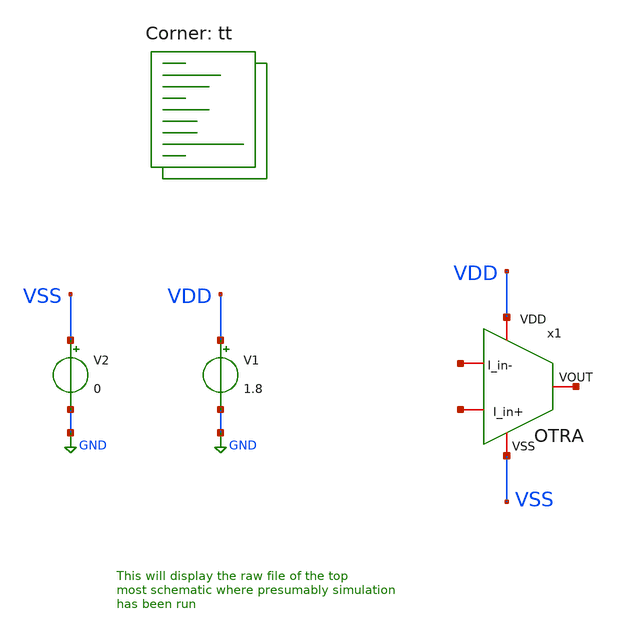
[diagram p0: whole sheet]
** sch_path: my_ip/sky130A/OTRA_VGA/testbenches/tb.sch
**.subckt tb
V1 VDD GND 1.8
V2 VSS GND 0
x1 VDD VSS net1 net2 net3 OTRA
**** begin user architecture code
.lib $::SKYWATER_MODELS/sky130.lib.spice tt
**** end user architecture code
**.ends
.GLOBAL GND
**** begin user architecture code


* ngspice commands
.options savecurrents
.TEMP 27
.control
save all
save @m.x1.xm1.msky130_fd_pr__pfet_01v8_lvt[gm]
save @m.x1.xm1.msky130_fd_pr__pfet_01v8_lvt[vth]
save @m.x1.xm1.msky130_fd_pr__pfet_01v8_lvt[gds]
save @m.x1.xm1.msky130_fd_pr__pfet_01v8_lvt[gmbs]
save @m.x1.xm1.msky130_fd_pr__pfet_01v8_lvt[vds]
save @m.x1.xm1.msky130_fd_pr__pfet_01v8_lvt[vgs]


save @m.x1.xm2.msky130_fd_pr__pfet_01v8_lvt[gm]
save @m.x1.xm2.msky130_fd_pr__pfet_01v8_lvt[vth]
save @m.x1.xm2.msky130_fd_pr__pfet_01v8_lvt[gds]
save @m.x1.xm2.msky130_fd_pr__pfet_01v8_lvt[gmbs]
save @m.x1.xm2.msky130_fd_pr__pfet_01v8_lvt[vds]
save @m.x1.xm2.msky130_fd_pr__pfet_01v8_lvt[vgs]

save @m.x1.xm3.msky130_fd_pr__nfet_01v8[gm]
save @m.x1.xm3.msky130_fd_pr__nfet_01v8[vth]
save @m.x1.xm3.msky130_fd_pr__nfet_01v8[gds]
save @m.x1.xm3.msky130_fd_pr__nfet_01v8[gmbs]
save @m.x1.xm3.msky130_fd_pr__nfet_01v8[vds]
save @m.x1.xm3.msky130_fd_pr__nfet_01v8[vgs]

save @m.x1.xm4.msky130_fd_pr__nfet_01v8[gm]
save @m.x1.xm4.msky130_fd_pr__nfet_01v8[vth]
save @m.x1.xm4.msky130_fd_pr__nfet_01v8[gds]
save @m.x1.xm4.msky130_fd_pr__nfet_01v8[gmbs]
save @m.x1.xm4.msky130_fd_pr__nfet_01v8[vds]
save @m.x1.xm4.msky130_fd_pr__nfet_01v8[vgs]

save @m.x1.xm5.msky130_fd_pr__nfet_01v8[gm]
save @m.x1.xm5.msky130_fd_pr__nfet_01v8[vth]
save @m.x1.xm5.msky130_fd_pr__nfet_01v8[gds]
save @m.x1.xm5.msky130_fd_pr__nfet_01v8[gmbs]
save @m.x1.xm5.msky130_fd_pr__nfet_01v8[vds]
save @m.x1.xm5.msky130_fd_pr__nfet_01v8[vgs]

save @m.x1.xm6.msky130_fd_pr__nfet_01v8[gm]
save @m.x1.xm6.msky130_fd_pr__nfet_01v8[vth]
save @m.x1.xm6.msky130_fd_pr__nfet_01v8[gds]
save @m.x1.xm6.msky130_fd_pr__nfet_01v8[gmbs]
save @m.x1.xm6.msky130_fd_pr__nfet_01v8[vds]
save @m.x1.xm6.msky130_fd_pr__nfet_01v8[vgs]


save @m.x1.xm7.msky130_fd_pr__pfet_01v8_lvt[gm]
save @m.x1.xm7.msky130_fd_pr__pfet_01v8_lvt[vth]
save @m.x1.xm7.msky130_fd_pr__pfet_01v8_lvt[gds]
save @m.x1.xm7.msky130_fd_pr__pfet_01v8_lvt[gmbs]
save @m.x1.xm7.msky130_fd_pr__pfet_01v8_lvt[vds]
save @m.x1.xm7.msky130_fd_pr__pfet_01v8_lvt[vgs]

save @m.x1.xm8.msky130_fd_pr__nfet_01v8[gm]
save @m.x1.xm8.msky130_fd_pr__nfet_01v8[vth]
save @m.x1.xm8.msky130_fd_pr__nfet_01v8[gds]
save @m.x1.xm8.msky130_fd_pr__nfet_01v8[gmbs]
save @m.x1.xm8.msky130_fd_pr__nfet_01v8[vds]
save @m.x1.xm8.msky130_fd_pr__nfet_01v8[vgs]

op
write tb.raw

.endc



**** end user architecture code
.end
